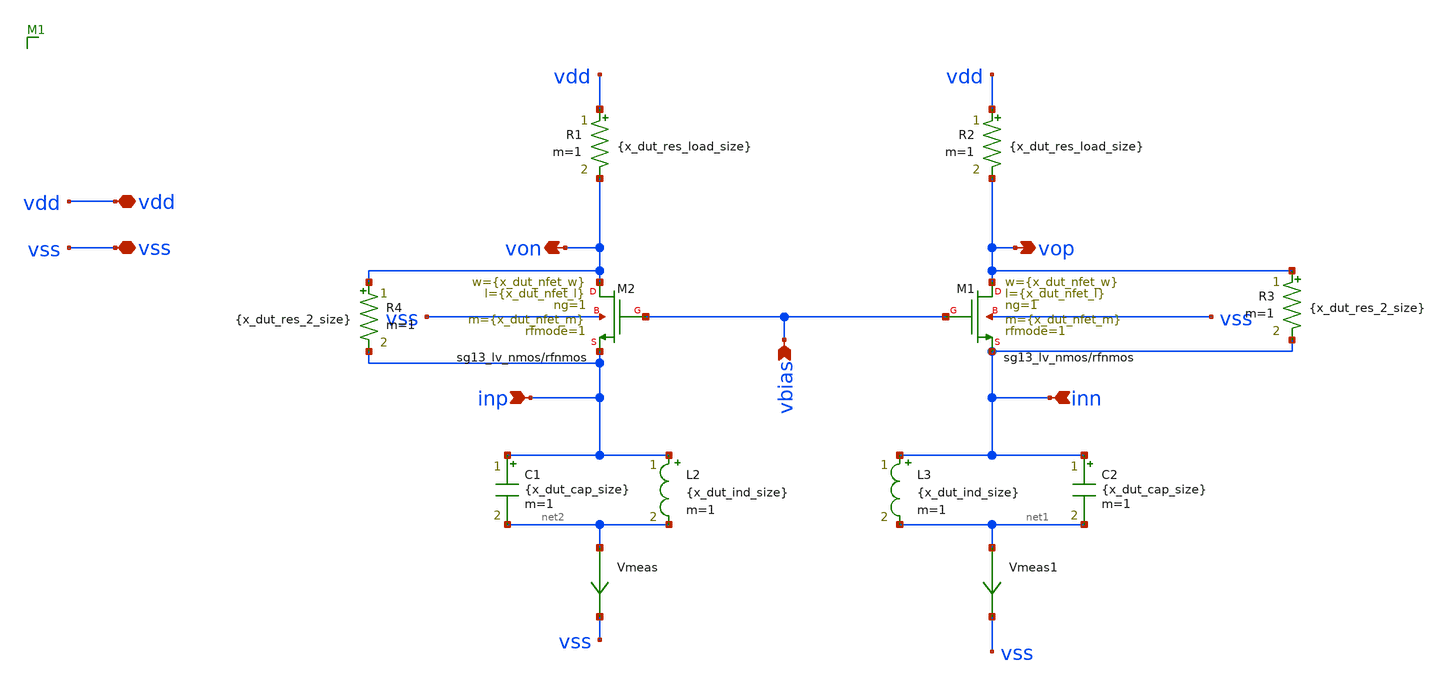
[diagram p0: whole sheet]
** sch_path: examples/tunable-tia/ihp-sg13g2/xschem/tia-topo-2/tia-bpf-2-ideal-comp.sch
**.subckt tia-bpf-2-ideal-comp vdd vss inp inn von vop vbias
*.iopin vdd
*.iopin vss
*.ipin inp
*.ipin inn
*.opin von
*.opin vop
*.ipin vbias
XM1 vop vbias inn vss sg13_lv_nmos w={x_dut_nfet_w} l={x_dut_nfet_l} ng=1 m={x_dut_nfet_m} rfmode=1 mm_ok=1
XM2 von vbias inp vss sg13_lv_nmos w={x_dut_nfet_w} l={x_dut_nfet_l} ng=1 m={x_dut_nfet_m} rfmode=1 mm_ok=1
L2 inp net2 {x_dut_ind_size} m=1
L3 inn net1 {x_dut_ind_size} m=1
C1 inp net2 {x_dut_cap_size} m=1
C2 inn net1 {x_dut_cap_size} m=1
R1 vdd von {x_dut_res_load_size} m=1
R2 vdd vop {x_dut_res_load_size} m=1
R3 vop inn {x_dut_res_2_size} m=1
R4 von inp {x_dut_res_2_size} m=1
Vmeas net2 vss 0
.save i(vmeas)
Vmeas1 net1 vss 0
.save i(vmeas1)
**.ends
.end
